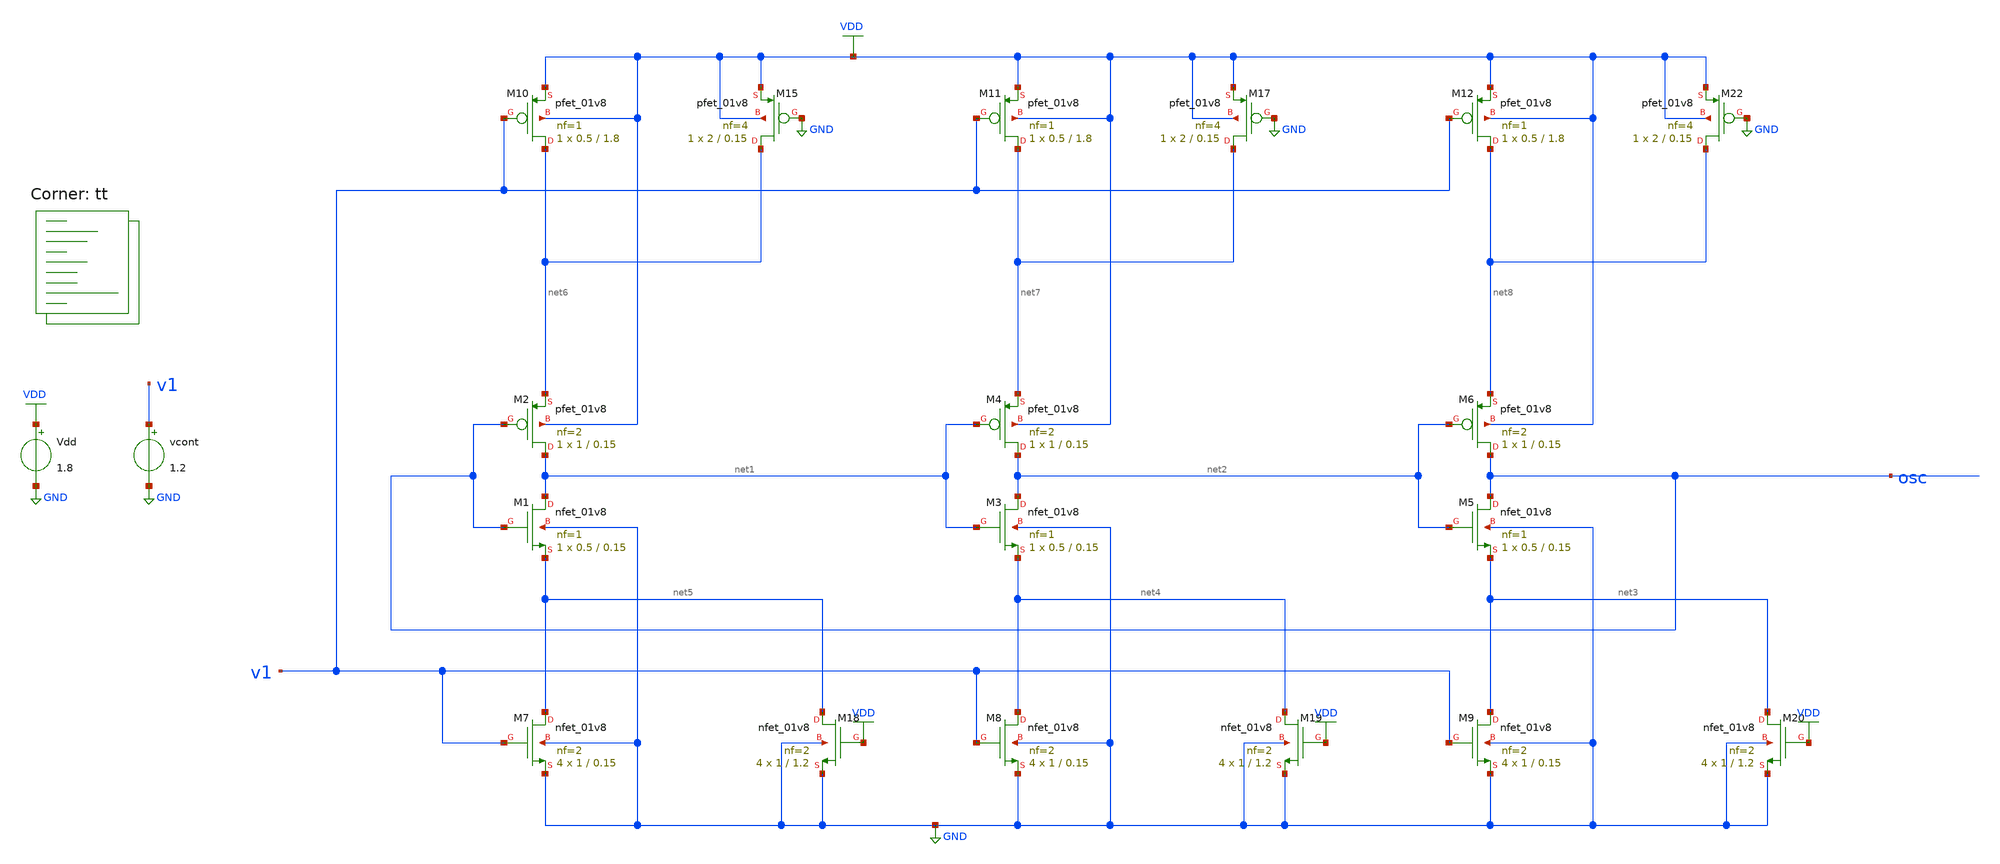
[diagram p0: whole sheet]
** sch_path: projects/pll/vco/xschem_ngspice/tb_current_starved_VCO4.sch
**.subckt tb_current_starved_VCO4
XM1 net1 osc net5 GND sky130_fd_pr__nfet_01v8 L=0.15 W=0.5 nf=1 ad='int((nf+1)/2) * W/nf * 0.29' as='int((nf+2)/2) * W/nf * 0.29'
+ pd='2*int((nf+1)/2) * (W/nf + 0.29)' ps='2*int((nf+2)/2) * (W/nf + 0.29)' nrd='0.29 / W' nrs='0.29 / W'
+ sa=0 sb=0 sd=0 mult=1 m=1
XM2 net1 osc net6 VDD sky130_fd_pr__pfet_01v8 L=0.15 W=1 nf=2 ad='int((nf+1)/2) * W/nf * 0.29' as='int((nf+2)/2) * W/nf * 0.29'
+ pd='2*int((nf+1)/2) * (W/nf + 0.29)' ps='2*int((nf+2)/2) * (W/nf + 0.29)' nrd='0.29 / W' nrs='0.29 / W'
+ sa=0 sb=0 sd=0 mult=1 m=1
XM3 net2 net1 net4 GND sky130_fd_pr__nfet_01v8 L=0.15 W=0.5 nf=1 ad='int((nf+1)/2) * W/nf * 0.29' as='int((nf+2)/2) * W/nf * 0.29'
+ pd='2*int((nf+1)/2) * (W/nf + 0.29)' ps='2*int((nf+2)/2) * (W/nf + 0.29)' nrd='0.29 / W' nrs='0.29 / W'
+ sa=0 sb=0 sd=0 mult=1 m=1
XM4 net2 net1 net7 VDD sky130_fd_pr__pfet_01v8 L=0.15 W=1 nf=2 ad='int((nf+1)/2) * W/nf * 0.29' as='int((nf+2)/2) * W/nf * 0.29'
+ pd='2*int((nf+1)/2) * (W/nf + 0.29)' ps='2*int((nf+2)/2) * (W/nf + 0.29)' nrd='0.29 / W' nrs='0.29 / W'
+ sa=0 sb=0 sd=0 mult=1 m=1
XM5 osc net2 net3 GND sky130_fd_pr__nfet_01v8 L=0.15 W=0.5 nf=1 ad='int((nf+1)/2) * W/nf * 0.29' as='int((nf+2)/2) * W/nf * 0.29'
+ pd='2*int((nf+1)/2) * (W/nf + 0.29)' ps='2*int((nf+2)/2) * (W/nf + 0.29)' nrd='0.29 / W' nrs='0.29 / W'
+ sa=0 sb=0 sd=0 mult=1 m=1
XM6 osc net2 net8 VDD sky130_fd_pr__pfet_01v8 L=0.15 W=1 nf=2 ad='int((nf+1)/2) * W/nf * 0.29' as='int((nf+2)/2) * W/nf * 0.29'
+ pd='2*int((nf+1)/2) * (W/nf + 0.29)' ps='2*int((nf+2)/2) * (W/nf + 0.29)' nrd='0.29 / W' nrs='0.29 / W'
+ sa=0 sb=0 sd=0 mult=1 m=1
XM7 net5 v1 GND GND sky130_fd_pr__nfet_01v8 L=0.15 W=1 nf=2 ad='int((nf+1)/2) * W/nf * 0.29' as='int((nf+2)/2) * W/nf * 0.29'
+ pd='2*int((nf+1)/2) * (W/nf + 0.29)' ps='2*int((nf+2)/2) * (W/nf + 0.29)' nrd='0.29 / W' nrs='0.29 / W'
+ sa=0 sb=0 sd=0 mult=4 m=4
XM8 net4 v1 GND GND sky130_fd_pr__nfet_01v8 L=0.15 W=1 nf=2 ad='int((nf+1)/2) * W/nf * 0.29' as='int((nf+2)/2) * W/nf * 0.29'
+ pd='2*int((nf+1)/2) * (W/nf + 0.29)' ps='2*int((nf+2)/2) * (W/nf + 0.29)' nrd='0.29 / W' nrs='0.29 / W'
+ sa=0 sb=0 sd=0 mult=4 m=4
XM9 net3 v1 GND GND sky130_fd_pr__nfet_01v8 L=0.15 W=1 nf=2 ad='int((nf+1)/2) * W/nf * 0.29' as='int((nf+2)/2) * W/nf * 0.29'
+ pd='2*int((nf+1)/2) * (W/nf + 0.29)' ps='2*int((nf+2)/2) * (W/nf + 0.29)' nrd='0.29 / W' nrs='0.29 / W'
+ sa=0 sb=0 sd=0 mult=4 m=4
XM10 net6 v1 VDD VDD sky130_fd_pr__pfet_01v8 L=1.8 W=0.5 nf=1 ad='int((nf+1)/2) * W/nf * 0.29' as='int((nf+2)/2) * W/nf * 0.29'
+ pd='2*int((nf+1)/2) * (W/nf + 0.29)' ps='2*int((nf+2)/2) * (W/nf + 0.29)' nrd='0.29 / W' nrs='0.29 / W'
+ sa=0 sb=0 sd=0 mult=1 m=1
XM11 net7 v1 VDD VDD sky130_fd_pr__pfet_01v8 L=1.8 W=0.5 nf=1 ad='int((nf+1)/2) * W/nf * 0.29' as='int((nf+2)/2) * W/nf * 0.29'
+ pd='2*int((nf+1)/2) * (W/nf + 0.29)' ps='2*int((nf+2)/2) * (W/nf + 0.29)' nrd='0.29 / W' nrs='0.29 / W'
+ sa=0 sb=0 sd=0 mult=1 m=1
XM12 net8 v1 VDD VDD sky130_fd_pr__pfet_01v8 L=1.8 W=0.5 nf=1 ad='int((nf+1)/2) * W/nf * 0.29' as='int((nf+2)/2) * W/nf * 0.29'
+ pd='2*int((nf+1)/2) * (W/nf + 0.29)' ps='2*int((nf+2)/2) * (W/nf + 0.29)' nrd='0.29 / W' nrs='0.29 / W'
+ sa=0 sb=0 sd=0 mult=1 m=1
Vdd VDD GND 1.8
vcont v1 GND 1.2
XM18 net5 VDD GND GND sky130_fd_pr__nfet_01v8 L=1.2 W=1 nf=2 ad='int((nf+1)/2) * W/nf * 0.29' as='int((nf+2)/2) * W/nf * 0.29'
+ pd='2*int((nf+1)/2) * (W/nf + 0.29)' ps='2*int((nf+2)/2) * (W/nf + 0.29)' nrd='0.29 / W' nrs='0.29 / W'
+ sa=0 sb=0 sd=0 mult=4 m=4
XM19 net4 VDD GND GND sky130_fd_pr__nfet_01v8 L=1.2 W=1 nf=2 ad='int((nf+1)/2) * W/nf * 0.29' as='int((nf+2)/2) * W/nf * 0.29'
+ pd='2*int((nf+1)/2) * (W/nf + 0.29)' ps='2*int((nf+2)/2) * (W/nf + 0.29)' nrd='0.29 / W' nrs='0.29 / W'
+ sa=0 sb=0 sd=0 mult=4 m=4
XM20 net3 VDD GND GND sky130_fd_pr__nfet_01v8 L=1.2 W=1 nf=2 ad='int((nf+1)/2) * W/nf * 0.29' as='int((nf+2)/2) * W/nf * 0.29'
+ pd='2*int((nf+1)/2) * (W/nf + 0.29)' ps='2*int((nf+2)/2) * (W/nf + 0.29)' nrd='0.29 / W' nrs='0.29 / W'
+ sa=0 sb=0 sd=0 mult=4 m=4
XM15 net6 GND VDD VDD sky130_fd_pr__pfet_01v8 L=0.15 W=2 nf=4 ad='int((nf+1)/2) * W/nf * 0.29' as='int((nf+2)/2) * W/nf * 0.29'
+ pd='2*int((nf+1)/2) * (W/nf + 0.29)' ps='2*int((nf+2)/2) * (W/nf + 0.29)' nrd='0.29 / W' nrs='0.29 / W'
+ sa=0 sb=0 sd=0 mult=1 m=1
XM17 net7 GND VDD VDD sky130_fd_pr__pfet_01v8 L=0.15 W=2 nf=4 ad='int((nf+1)/2) * W/nf * 0.29' as='int((nf+2)/2) * W/nf * 0.29'
+ pd='2*int((nf+1)/2) * (W/nf + 0.29)' ps='2*int((nf+2)/2) * (W/nf + 0.29)' nrd='0.29 / W' nrs='0.29 / W'
+ sa=0 sb=0 sd=0 mult=1 m=1
XM22 net8 GND VDD VDD sky130_fd_pr__pfet_01v8 L=0.15 W=2 nf=4 ad='int((nf+1)/2) * W/nf * 0.29' as='int((nf+2)/2) * W/nf * 0.29'
+ pd='2*int((nf+1)/2) * (W/nf + 0.29)' ps='2*int((nf+2)/2) * (W/nf + 0.29)' nrd='0.29 / W' nrs='0.29 / W'
+ sa=0 sb=0 sd=0 mult=1 m=1
**** begin user architecture code
.lib $::SKYWATER_MODELS/sky130.lib.spice tt



.option method=gear
.option wnflag=1


*.ic v(vcont)=1.2

*.temp = 75

* Xmeasure osc freq2 measure_Kvco thresh=0.9 dir=1

.control

  * pre_osdi ./measure_Kvco.osdi

  let v_cont_start = 0.0
  let v_cont_stop = 1.9

  dowhile v_cont_start <= v_cont_stop
    alter vcont $&v_cont_start
    save v(vcont) v(osc) v(vout) v(v1) v(v2) i(vmeas) i(vmeas1)
    *save all
    tran 1ps 30ns
    remzerovec
    write tb_current_starved_VCO4_{$&v_cont_start}.raw
    * write tb_current_starved_VCO4.raw
    linearize v(osc)
    let filename = v_cont_start * 100
    wrdata /foss/designs/my_design/projects/pll/vco/xschem_ngspice/tb_current_starved_VCO4_{$&filename}.txt
+ v(osc)
    set appendwrite

    reset
    let v_cont_start = v_cont_start + 0.1
  end
.endc




**** end user architecture code
**.ends
.GLOBAL VDD
.GLOBAL GND
.end
